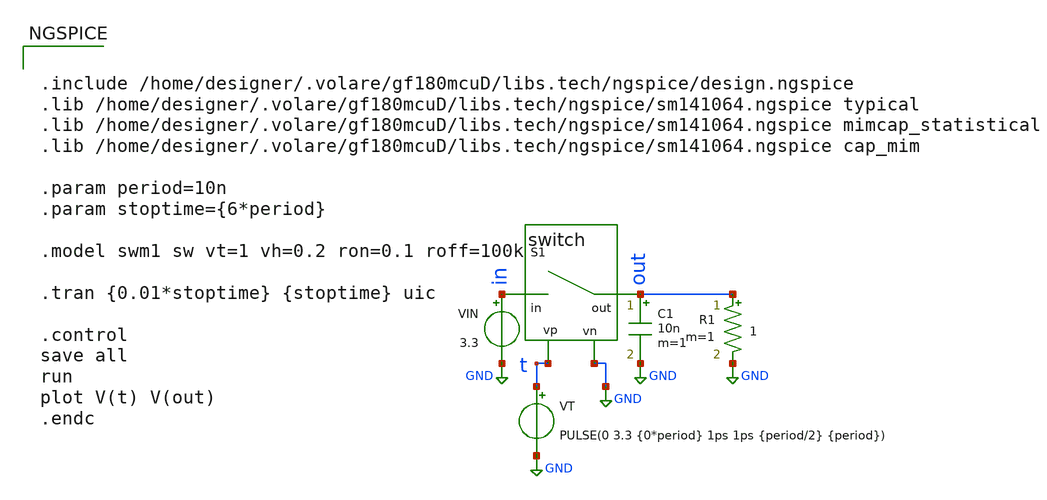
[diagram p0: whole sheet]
** sch_path: SAR_ADC/xschem/test/tb_switch.sch
**.subckt tb_switch
S1 in out t GND swm1
C1 out GND 10n m=1
VIN in GND 3.3
VT t GND PULSE(0 3.3 {0*period} 1ps 1ps {period/2} {period})
R1 out GND 1 m=1
**** begin user architecture code


.include /home/designer/.volare/gf180mcuD/libs.tech/ngspice/design.ngspice
.lib /home/designer/.volare/gf180mcuD/libs.tech/ngspice/sm141064.ngspice typical
.lib /home/designer/.volare/gf180mcuD/libs.tech/ngspice/sm141064.ngspice mimcap_statistical
.lib /home/designer/.volare/gf180mcuD/libs.tech/ngspice/sm141064.ngspice cap_mim

.param period=10n
.param stoptime={6*period}

.model swm1 sw vt=1 vh=0.2 ron=0.1 roff=100k

.tran {0.01*stoptime} {stoptime} uic

.control
save all
run
plot V(t) V(out)
.endc


**** end user architecture code
**.ends
.GLOBAL GND
.end
